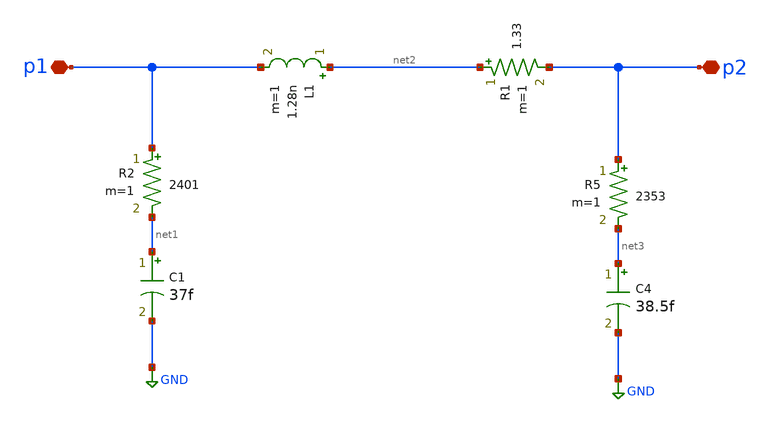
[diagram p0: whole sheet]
** sch_path: LNA7096-main/schematic/xschem/01_lna/ls.sch
**.subckt ls p1 p2
*.iopin p1
*.iopin p2
L1 net2 p1 1.28n m=1
R1 net2 p2 1.33 m=1
R2 p1 net1 2401 m=1
C1 net1 GND 37f m=1
R5 p2 net3 2353 m=1
C4 net3 GND 38.5f m=1
**.ends
.GLOBAL GND
.end
